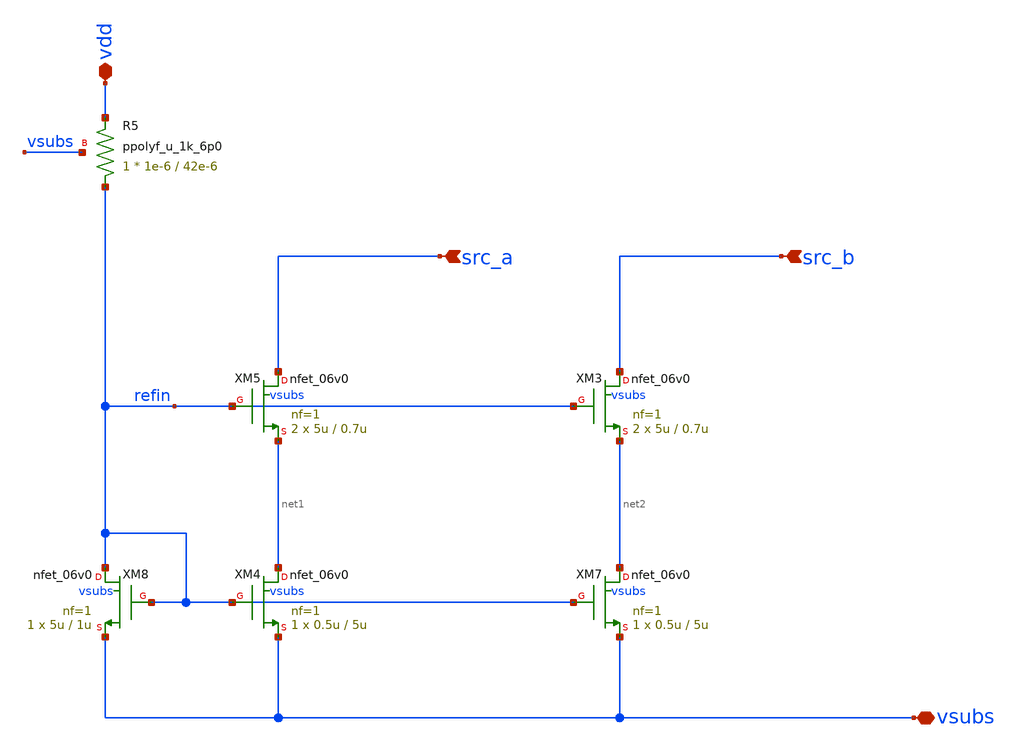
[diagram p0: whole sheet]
** sch_path: xschem/ip_current_source.sch
**.subckt ip_current_source vdd vsubs src_a src_b
*.iopin vdd
*.iopin vsubs
*.ipin src_a
*.ipin src_b
XM8 refin refin vsubs vsubs nfet_06v0 L=1u W=5u nf=1 ad='int((nf+1)/2) * W/nf * 0.18u' as='int((nf+2)/2) * W/nf * 0.18u'
+ pd='2*int((nf+1)/2) * (W/nf + 0.18u)' ps='2*int((nf+2)/2) * (W/nf + 0.18u)' nrd='0.18u / W' nrs='0.18u / W'
+ sa=0 sb=0 sd=0 m=1 par=1
XM5 src_a refin net1 vsubs nfet_06v0 L=0.7u W=5u nf=1 ad='int((nf+1)/2) * W/nf * 0.18u' as='int((nf+2)/2) * W/nf * 0.18u'
+ pd='2*int((nf+1)/2) * (W/nf + 0.18u)' ps='2*int((nf+2)/2) * (W/nf + 0.18u)' nrd='0.18u / W' nrs='0.18u / W'
+ sa=0 sb=0 sd=0 m=2 par=2
XM3 src_b refin net2 vsubs nfet_06v0 L=0.7u W=5u nf=1 ad='int((nf+1)/2) * W/nf * 0.18u' as='int((nf+2)/2) * W/nf * 0.18u'
+ pd='2*int((nf+1)/2) * (W/nf + 0.18u)' ps='2*int((nf+2)/2) * (W/nf + 0.18u)' nrd='0.18u / W' nrs='0.18u / W'
+ sa=0 sb=0 sd=0 m=2 par=2
XM4 net1 refin vsubs vsubs nfet_06v0 L=5u W=0.5u nf=1 ad='int((nf+1)/2) * W/nf * 0.18u' as='int((nf+2)/2) * W/nf * 0.18u'
+ pd='2*int((nf+1)/2) * (W/nf + 0.18u)' ps='2*int((nf+2)/2) * (W/nf + 0.18u)' nrd='0.18u / W' nrs='0.18u / W'
+ sa=0 sb=0 sd=0 m=1 par=1
XM7 net2 refin vsubs vsubs nfet_06v0 L=5u W=0.5u nf=1 ad='int((nf+1)/2) * W/nf * 0.18u' as='int((nf+2)/2) * W/nf * 0.18u'
+ pd='2*int((nf+1)/2) * (W/nf + 0.18u)' ps='2*int((nf+2)/2) * (W/nf + 0.18u)' nrd='0.18u / W' nrs='0.18u / W'
+ sa=0 sb=0 sd=0 m=1 par=1
XR5 refin vdd vsubs ppolyf_u_1k_6p0 r_width=1e-6 r_length=42e-6 m=1
**.ends
.end
